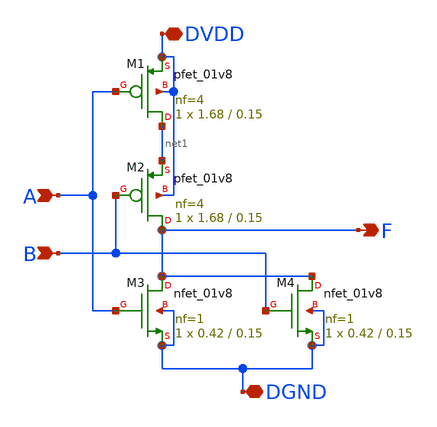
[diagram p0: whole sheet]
** sch_path: mywork/nor2x1/nor2x1.sch
**.subckt nor2x1 DVDD DGND A F B
*.iopin DVDD
*.iopin DGND
*.ipin A
*.opin F
*.ipin B
XM1 net1 A DVDD DVDD sky130_fd_pr__pfet_01v8 L=0.15 W=1.68 nf=4 ad='int((nf+1)/2) * W/nf * 0.29' as='int((nf+2)/2) * W/nf * 0.29'
+ pd='2*int((nf+1)/2) * (W/nf + 0.29)' ps='2*int((nf+2)/2) * (W/nf + 0.29)' nrd='0.29 / W' nrs='0.29 / W'
+ sa=0 sb=0 sd=0 mult=1 m=1
XM2 F B net1 DVDD sky130_fd_pr__pfet_01v8 L=0.15 W=1.68 nf=4 ad='int((nf+1)/2) * W/nf * 0.29' as='int((nf+2)/2) * W/nf * 0.29'
+ pd='2*int((nf+1)/2) * (W/nf + 0.29)' ps='2*int((nf+2)/2) * (W/nf + 0.29)' nrd='0.29 / W' nrs='0.29 / W'
+ sa=0 sb=0 sd=0 mult=1 m=1
XM3 F A DGND DGND sky130_fd_pr__nfet_01v8 L=0.15 W=0.42 nf=1 ad='int((nf+1)/2) * W/nf * 0.29' as='int((nf+2)/2) * W/nf * 0.29'
+ pd='2*int((nf+1)/2) * (W/nf + 0.29)' ps='2*int((nf+2)/2) * (W/nf + 0.29)' nrd='0.29 / W' nrs='0.29 / W'
+ sa=0 sb=0 sd=0 mult=1 m=1
XM4 F B DGND DGND sky130_fd_pr__nfet_01v8 L=0.15 W=0.42 nf=1 ad='int((nf+1)/2) * W/nf * 0.29' as='int((nf+2)/2) * W/nf * 0.29'
+ pd='2*int((nf+1)/2) * (W/nf + 0.29)' ps='2*int((nf+2)/2) * (W/nf + 0.29)' nrd='0.29 / W' nrs='0.29 / W'
+ sa=0 sb=0 sd=0 mult=1 m=1
**.ends
.end
